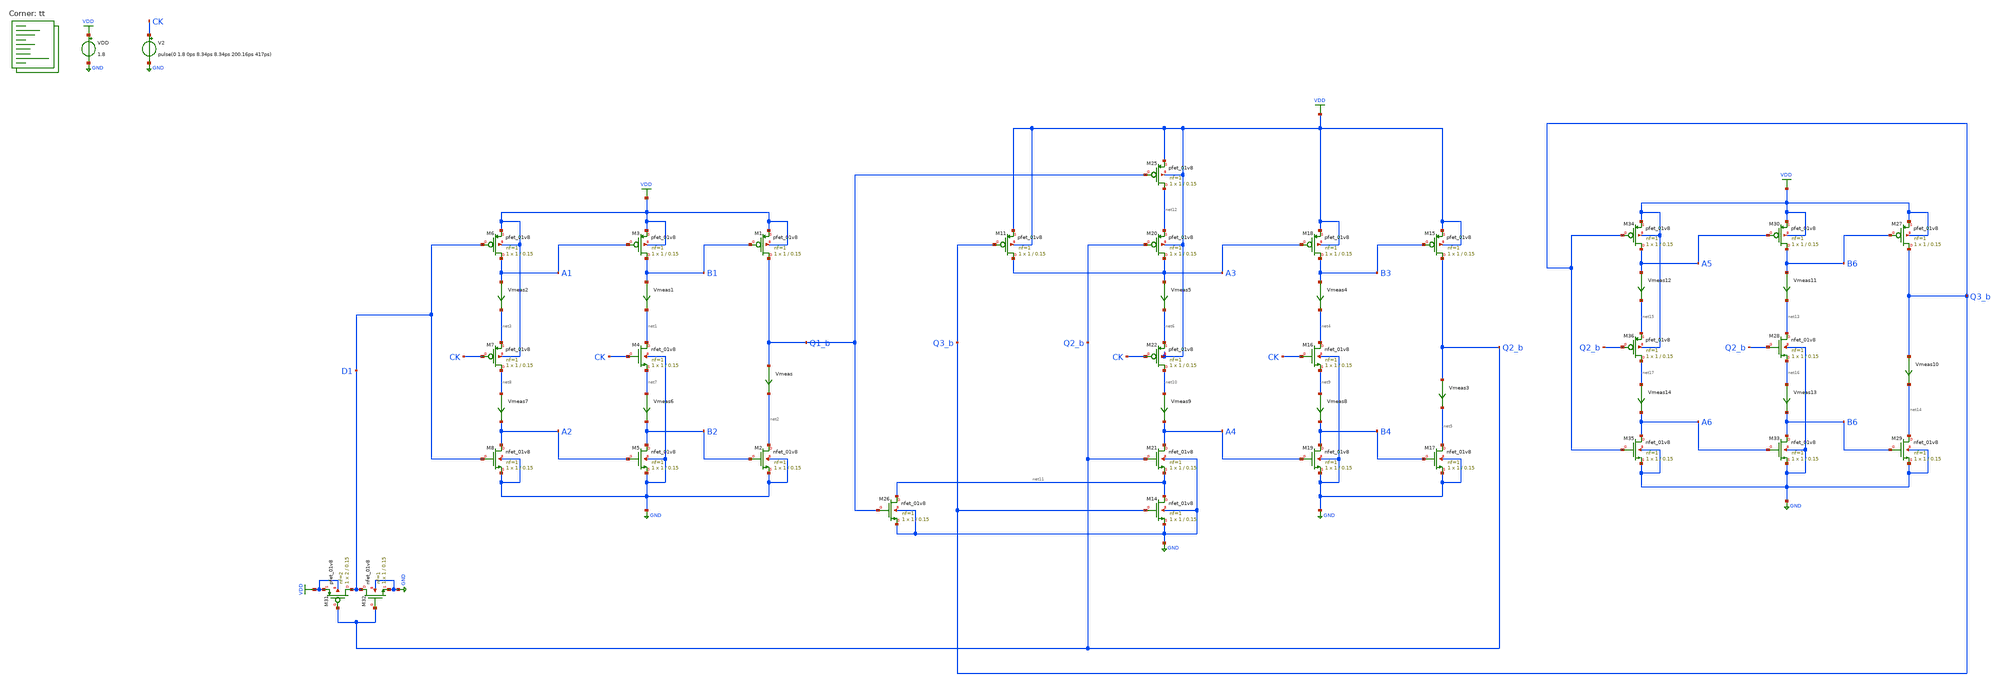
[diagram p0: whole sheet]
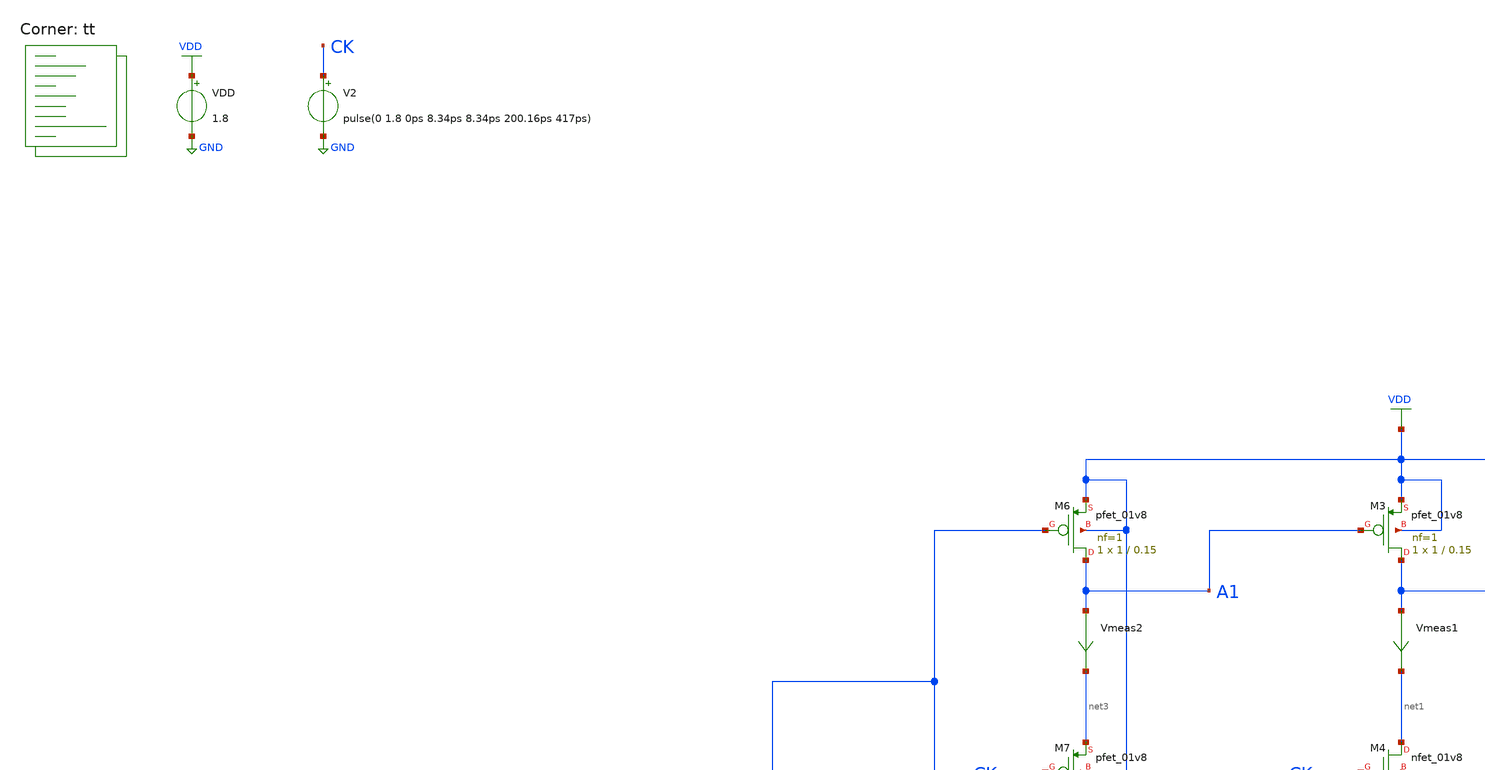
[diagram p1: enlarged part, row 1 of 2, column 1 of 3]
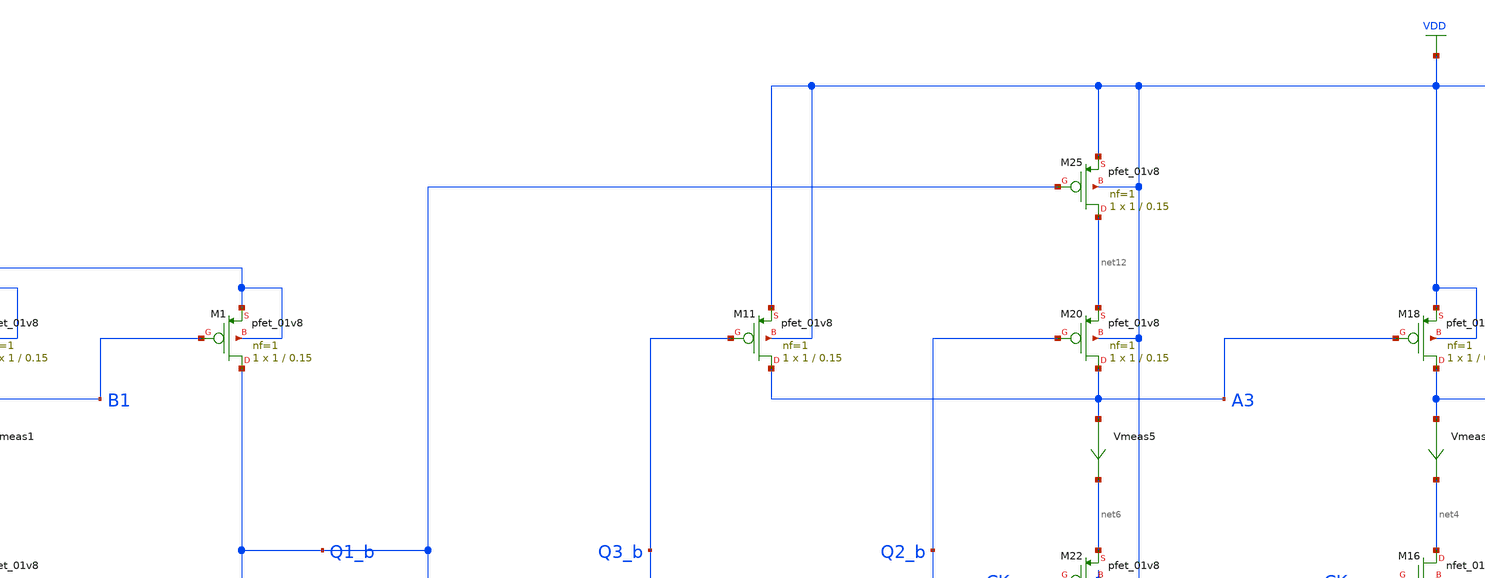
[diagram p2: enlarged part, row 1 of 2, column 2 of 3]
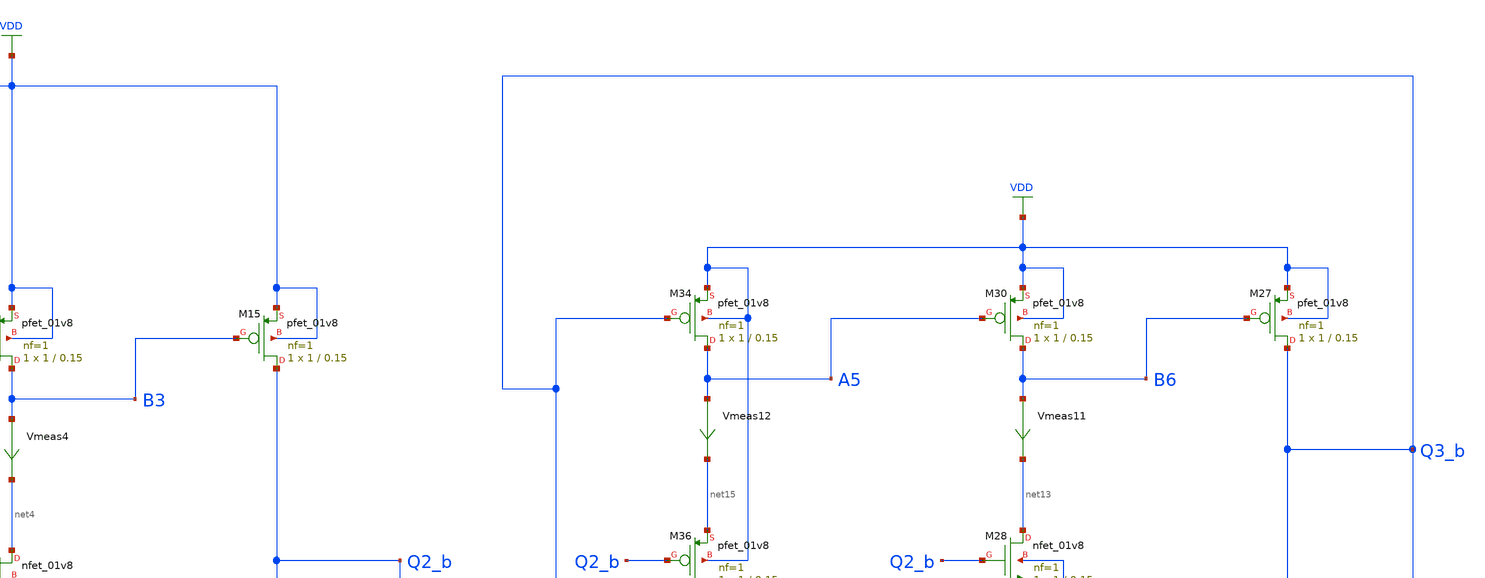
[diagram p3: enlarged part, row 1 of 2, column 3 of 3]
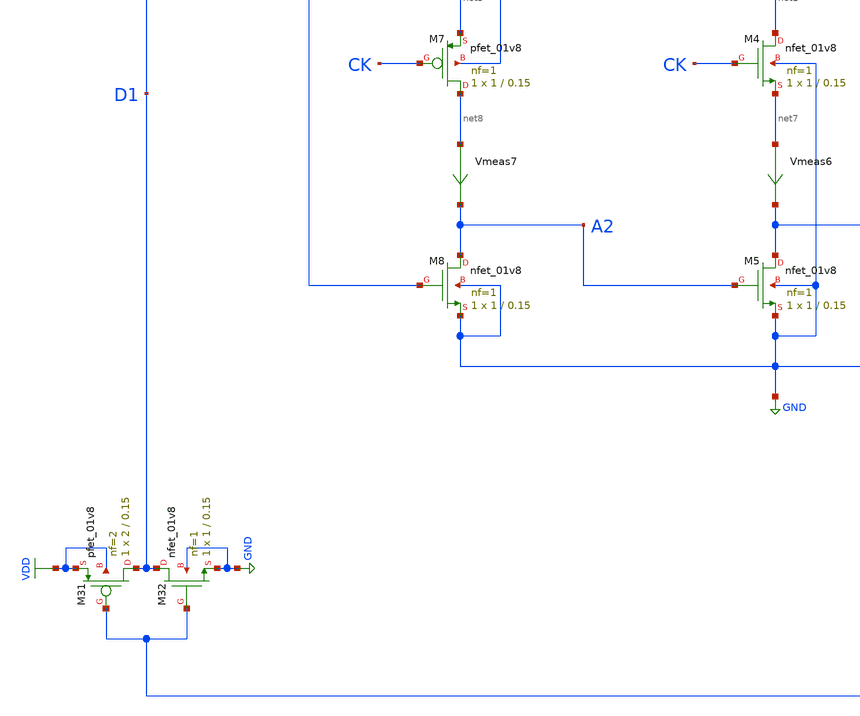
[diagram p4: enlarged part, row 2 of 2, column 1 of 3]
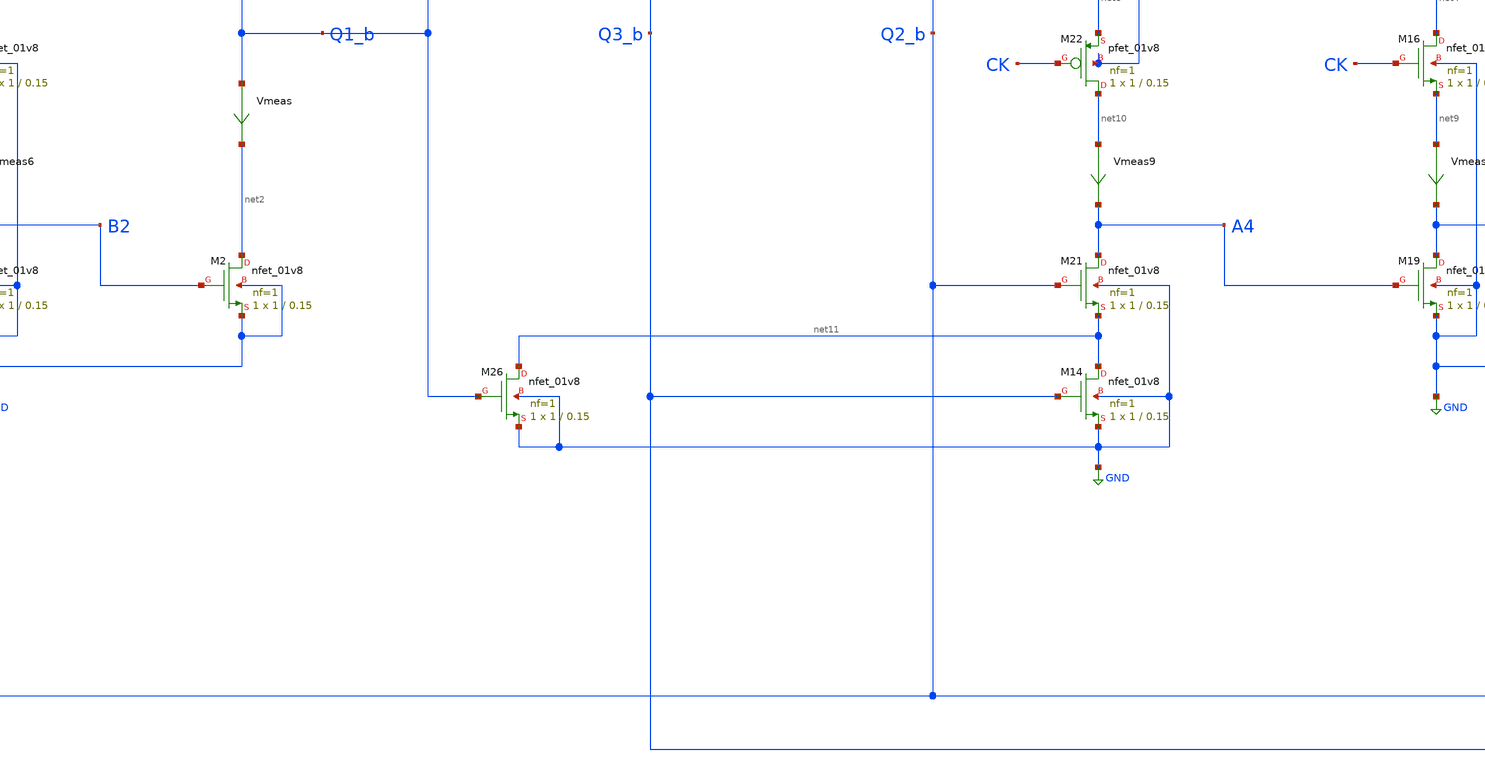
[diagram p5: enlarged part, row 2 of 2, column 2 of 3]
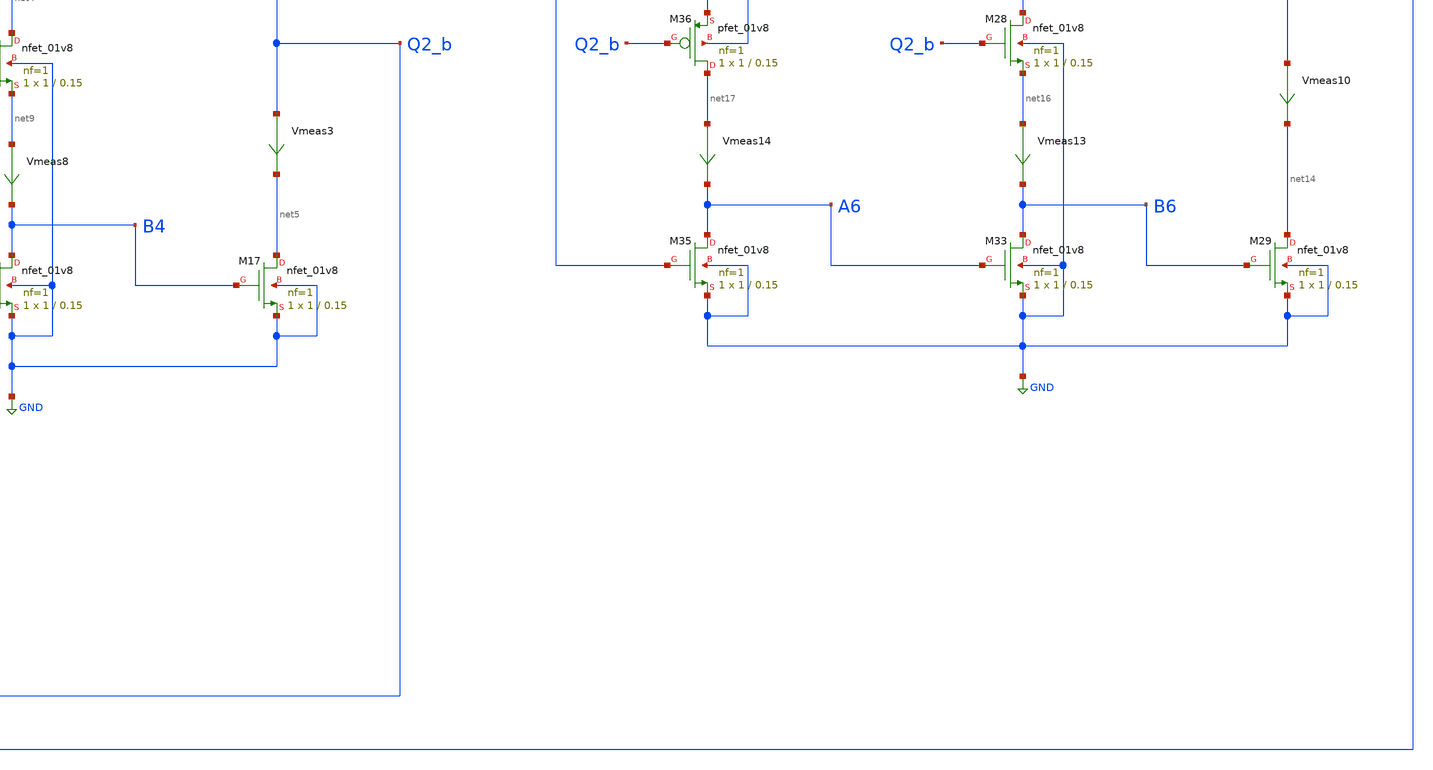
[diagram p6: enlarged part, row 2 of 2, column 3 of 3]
** sch_path: projects/pll/divider/xschem_ngspice/tb_TSPC_FF_comp_sw_divide3_6.sch
**.subckt tb_TSPC_FF_comp_sw_divide3_6
VDD VDD GND 1.8
XM1 Q1_b B1 VDD VDD sky130_fd_pr__pfet_01v8 L=0.15 W=1 nf=1 ad='int((nf+1)/2) * W/nf * 0.29' as='int((nf+2)/2) * W/nf * 0.29'
+ pd='2*int((nf+1)/2) * (W/nf + 0.29)' ps='2*int((nf+2)/2) * (W/nf + 0.29)' nrd='0.29 / W' nrs='0.29 / W'
+ sa=0 sb=0 sd=0 mult=1 m=1
XM4 net1 CK net7 GND sky130_fd_pr__nfet_01v8 L=0.15 W=1 nf=1 ad='int((nf+1)/2) * W/nf * 0.29' as='int((nf+2)/2) * W/nf * 0.29'
+ pd='2*int((nf+1)/2) * (W/nf + 0.29)' ps='2*int((nf+2)/2) * (W/nf + 0.29)' nrd='0.29 / W' nrs='0.29 / W'
+ sa=0 sb=0 sd=0 mult=1 m=1
Vmeas Q1_b net2 0
.save i(vmeas)
XM2 net2 B2 GND GND sky130_fd_pr__nfet_01v8 L=0.15 W=1 nf=1 ad='int((nf+1)/2) * W/nf * 0.29' as='int((nf+2)/2) * W/nf * 0.29'
+ pd='2*int((nf+1)/2) * (W/nf + 0.29)' ps='2*int((nf+2)/2) * (W/nf + 0.29)' nrd='0.29 / W' nrs='0.29 / W'
+ sa=0 sb=0 sd=0 mult=1 m=1
XM3 B1 A1 VDD VDD sky130_fd_pr__pfet_01v8 L=0.15 W=1 nf=1 ad='int((nf+1)/2) * W/nf * 0.29' as='int((nf+2)/2) * W/nf * 0.29'
+ pd='2*int((nf+1)/2) * (W/nf + 0.29)' ps='2*int((nf+2)/2) * (W/nf + 0.29)' nrd='0.29 / W' nrs='0.29 / W'
+ sa=0 sb=0 sd=0 mult=1 m=1
XM5 B2 A2 GND GND sky130_fd_pr__nfet_01v8 L=0.15 W=1 nf=1 ad='int((nf+1)/2) * W/nf * 0.29' as='int((nf+2)/2) * W/nf * 0.29'
+ pd='2*int((nf+1)/2) * (W/nf + 0.29)' ps='2*int((nf+2)/2) * (W/nf + 0.29)' nrd='0.29 / W' nrs='0.29 / W'
+ sa=0 sb=0 sd=0 mult=1 m=1
Vmeas1 B1 net1 0
.save i(vmeas1)
XM6 A1 D1 VDD VDD sky130_fd_pr__pfet_01v8 L=0.15 W=1 nf=1 ad='int((nf+1)/2) * W/nf * 0.29' as='int((nf+2)/2) * W/nf * 0.29'
+ pd='2*int((nf+1)/2) * (W/nf + 0.29)' ps='2*int((nf+2)/2) * (W/nf + 0.29)' nrd='0.29 / W' nrs='0.29 / W'
+ sa=0 sb=0 sd=0 mult=1 m=1
XM8 A2 D1 GND GND sky130_fd_pr__nfet_01v8 L=0.15 W=1 nf=1 ad='int((nf+1)/2) * W/nf * 0.29' as='int((nf+2)/2) * W/nf * 0.29'
+ pd='2*int((nf+1)/2) * (W/nf + 0.29)' ps='2*int((nf+2)/2) * (W/nf + 0.29)' nrd='0.29 / W' nrs='0.29 / W'
+ sa=0 sb=0 sd=0 mult=1 m=1
Vmeas2 A1 net3 0
.save i(vmeas2)
XM7 net8 CK net3 VDD sky130_fd_pr__pfet_01v8 L=0.15 W=1 nf=1 ad='int((nf+1)/2) * W/nf * 0.29' as='int((nf+2)/2) * W/nf * 0.29'
+ pd='2*int((nf+1)/2) * (W/nf + 0.29)' ps='2*int((nf+2)/2) * (W/nf + 0.29)' nrd='0.29 / W' nrs='0.29 / W'
+ sa=0 sb=0 sd=0 mult=1 m=1
XM15 Q2_b B3 VDD VDD sky130_fd_pr__pfet_01v8 L=0.15 W=1 nf=1 ad='int((nf+1)/2) * W/nf * 0.29' as='int((nf+2)/2) * W/nf * 0.29'
+ pd='2*int((nf+1)/2) * (W/nf + 0.29)' ps='2*int((nf+2)/2) * (W/nf + 0.29)' nrd='0.29 / W' nrs='0.29 / W'
+ sa=0 sb=0 sd=0 mult=1 m=1
XM16 net4 CK net9 GND sky130_fd_pr__nfet_01v8 L=0.15 W=1 nf=1 ad='int((nf+1)/2) * W/nf * 0.29' as='int((nf+2)/2) * W/nf * 0.29'
+ pd='2*int((nf+1)/2) * (W/nf + 0.29)' ps='2*int((nf+2)/2) * (W/nf + 0.29)' nrd='0.29 / W' nrs='0.29 / W'
+ sa=0 sb=0 sd=0 mult=1 m=1
Vmeas3 Q2_b net5 0
.save i(vmeas3)
XM17 net5 B4 GND GND sky130_fd_pr__nfet_01v8 L=0.15 W=1 nf=1 ad='int((nf+1)/2) * W/nf * 0.29' as='int((nf+2)/2) * W/nf * 0.29'
+ pd='2*int((nf+1)/2) * (W/nf + 0.29)' ps='2*int((nf+2)/2) * (W/nf + 0.29)' nrd='0.29 / W' nrs='0.29 / W'
+ sa=0 sb=0 sd=0 mult=1 m=1
XM18 B3 A3 VDD VDD sky130_fd_pr__pfet_01v8 L=0.15 W=1 nf=1 ad='int((nf+1)/2) * W/nf * 0.29' as='int((nf+2)/2) * W/nf * 0.29'
+ pd='2*int((nf+1)/2) * (W/nf + 0.29)' ps='2*int((nf+2)/2) * (W/nf + 0.29)' nrd='0.29 / W' nrs='0.29 / W'
+ sa=0 sb=0 sd=0 mult=1 m=1
XM19 B4 A4 GND GND sky130_fd_pr__nfet_01v8 L=0.15 W=1 nf=1 ad='int((nf+1)/2) * W/nf * 0.29' as='int((nf+2)/2) * W/nf * 0.29'
+ pd='2*int((nf+1)/2) * (W/nf + 0.29)' ps='2*int((nf+2)/2) * (W/nf + 0.29)' nrd='0.29 / W' nrs='0.29 / W'
+ sa=0 sb=0 sd=0 mult=1 m=1
Vmeas4 B3 net4 0
.save i(vmeas4)
XM20 A3 Q2_b net12 VDD sky130_fd_pr__pfet_01v8 L=0.15 W=1 nf=1 ad='int((nf+1)/2) * W/nf * 0.29' as='int((nf+2)/2) * W/nf * 0.29'
+ pd='2*int((nf+1)/2) * (W/nf + 0.29)' ps='2*int((nf+2)/2) * (W/nf + 0.29)' nrd='0.29 / W' nrs='0.29 / W'
+ sa=0 sb=0 sd=0 mult=1 m=1
XM21 A4 Q2_b net11 GND sky130_fd_pr__nfet_01v8 L=0.15 W=1 nf=1 ad='int((nf+1)/2) * W/nf * 0.29' as='int((nf+2)/2) * W/nf * 0.29'
+ pd='2*int((nf+1)/2) * (W/nf + 0.29)' ps='2*int((nf+2)/2) * (W/nf + 0.29)' nrd='0.29 / W' nrs='0.29 / W'
+ sa=0 sb=0 sd=0 mult=1 m=1
Vmeas5 A3 net6 0
.save i(vmeas5)
XM22 net10 CK net6 VDD sky130_fd_pr__pfet_01v8 L=0.15 W=1 nf=1 ad='int((nf+1)/2) * W/nf * 0.29' as='int((nf+2)/2) * W/nf * 0.29'
+ pd='2*int((nf+1)/2) * (W/nf + 0.29)' ps='2*int((nf+2)/2) * (W/nf + 0.29)' nrd='0.29 / W' nrs='0.29 / W'
+ sa=0 sb=0 sd=0 mult=1 m=1
Vmeas6 net7 B2 0
.save i(vmeas6)
Vmeas7 net8 A2 0
.save i(vmeas7)
Vmeas8 net9 B4 0
.save i(vmeas8)
Vmeas9 net10 A4 0
.save i(vmeas9)
V2 CK GND pulse(0 1.8 0ps 8.34ps 8.34ps 200.16ps 417ps)
XM31 D1 Q2_b VDD VDD sky130_fd_pr__pfet_01v8 L=0.15 W=2 nf=2 ad='int((nf+1)/2) * W/nf * 0.29' as='int((nf+2)/2) * W/nf * 0.29'
+ pd='2*int((nf+1)/2) * (W/nf + 0.29)' ps='2*int((nf+2)/2) * (W/nf + 0.29)' nrd='0.29 / W' nrs='0.29 / W'
+ sa=0 sb=0 sd=0 mult=1 m=1
XM32 D1 Q2_b GND GND sky130_fd_pr__nfet_01v8 L=0.15 W=1 nf=1 ad='int((nf+1)/2) * W/nf * 0.29' as='int((nf+2)/2) * W/nf * 0.29'
+ pd='2*int((nf+1)/2) * (W/nf + 0.29)' ps='2*int((nf+2)/2) * (W/nf + 0.29)' nrd='0.29 / W' nrs='0.29 / W'
+ sa=0 sb=0 sd=0 mult=1 m=1
XM11 A3 Q3_b VDD VDD sky130_fd_pr__pfet_01v8 L=0.15 W=1 nf=1 ad='int((nf+1)/2) * W/nf * 0.29' as='int((nf+2)/2) * W/nf * 0.29'
+ pd='2*int((nf+1)/2) * (W/nf + 0.29)' ps='2*int((nf+2)/2) * (W/nf + 0.29)' nrd='0.29 / W' nrs='0.29 / W'
+ sa=0 sb=0 sd=0 mult=1 m=1
XM14 net11 Q3_b GND GND sky130_fd_pr__nfet_01v8 L=0.15 W=1 nf=1 ad='int((nf+1)/2) * W/nf * 0.29' as='int((nf+2)/2) * W/nf * 0.29'
+ pd='2*int((nf+1)/2) * (W/nf + 0.29)' ps='2*int((nf+2)/2) * (W/nf + 0.29)' nrd='0.29 / W' nrs='0.29 / W'
+ sa=0 sb=0 sd=0 mult=1 m=1
XM25 net12 Q1_b VDD VDD sky130_fd_pr__pfet_01v8 L=0.15 W=1 nf=1 ad='int((nf+1)/2) * W/nf * 0.29' as='int((nf+2)/2) * W/nf * 0.29'
+ pd='2*int((nf+1)/2) * (W/nf + 0.29)' ps='2*int((nf+2)/2) * (W/nf + 0.29)' nrd='0.29 / W' nrs='0.29 / W'
+ sa=0 sb=0 sd=0 mult=1 m=1
XM26 net11 Q1_b GND GND sky130_fd_pr__nfet_01v8 L=0.15 W=1 nf=1 ad='int((nf+1)/2) * W/nf * 0.29' as='int((nf+2)/2) * W/nf * 0.29'
+ pd='2*int((nf+1)/2) * (W/nf + 0.29)' ps='2*int((nf+2)/2) * (W/nf + 0.29)' nrd='0.29 / W' nrs='0.29 / W'
+ sa=0 sb=0 sd=0 mult=1 m=1
XM27 Q3_b B6 VDD VDD sky130_fd_pr__pfet_01v8 L=0.15 W=1 nf=1 ad='int((nf+1)/2) * W/nf * 0.29' as='int((nf+2)/2) * W/nf * 0.29'
+ pd='2*int((nf+1)/2) * (W/nf + 0.29)' ps='2*int((nf+2)/2) * (W/nf + 0.29)' nrd='0.29 / W' nrs='0.29 / W'
+ sa=0 sb=0 sd=0 mult=1 m=1
XM28 net13 Q2_b net16 GND sky130_fd_pr__nfet_01v8 L=0.15 W=1 nf=1 ad='int((nf+1)/2) * W/nf * 0.29' as='int((nf+2)/2) * W/nf * 0.29'
+ pd='2*int((nf+1)/2) * (W/nf + 0.29)' ps='2*int((nf+2)/2) * (W/nf + 0.29)' nrd='0.29 / W' nrs='0.29 / W'
+ sa=0 sb=0 sd=0 mult=1 m=1
Vmeas10 Q3_b net14 0
.save i(vmeas10)
XM29 net14 B6 GND GND sky130_fd_pr__nfet_01v8 L=0.15 W=1 nf=1 ad='int((nf+1)/2) * W/nf * 0.29' as='int((nf+2)/2) * W/nf * 0.29'
+ pd='2*int((nf+1)/2) * (W/nf + 0.29)' ps='2*int((nf+2)/2) * (W/nf + 0.29)' nrd='0.29 / W' nrs='0.29 / W'
+ sa=0 sb=0 sd=0 mult=1 m=1
XM30 B6 A5 VDD VDD sky130_fd_pr__pfet_01v8 L=0.15 W=1 nf=1 ad='int((nf+1)/2) * W/nf * 0.29' as='int((nf+2)/2) * W/nf * 0.29'
+ pd='2*int((nf+1)/2) * (W/nf + 0.29)' ps='2*int((nf+2)/2) * (W/nf + 0.29)' nrd='0.29 / W' nrs='0.29 / W'
+ sa=0 sb=0 sd=0 mult=1 m=1
XM33 B6 A6 GND GND sky130_fd_pr__nfet_01v8 L=0.15 W=1 nf=1 ad='int((nf+1)/2) * W/nf * 0.29' as='int((nf+2)/2) * W/nf * 0.29'
+ pd='2*int((nf+1)/2) * (W/nf + 0.29)' ps='2*int((nf+2)/2) * (W/nf + 0.29)' nrd='0.29 / W' nrs='0.29 / W'
+ sa=0 sb=0 sd=0 mult=1 m=1
Vmeas11 B6 net13 0
.save i(vmeas11)
XM34 A5 Q3_b VDD VDD sky130_fd_pr__pfet_01v8 L=0.15 W=1 nf=1 ad='int((nf+1)/2) * W/nf * 0.29' as='int((nf+2)/2) * W/nf * 0.29'
+ pd='2*int((nf+1)/2) * (W/nf + 0.29)' ps='2*int((nf+2)/2) * (W/nf + 0.29)' nrd='0.29 / W' nrs='0.29 / W'
+ sa=0 sb=0 sd=0 mult=1 m=1
XM35 A6 Q3_b GND GND sky130_fd_pr__nfet_01v8 L=0.15 W=1 nf=1 ad='int((nf+1)/2) * W/nf * 0.29' as='int((nf+2)/2) * W/nf * 0.29'
+ pd='2*int((nf+1)/2) * (W/nf + 0.29)' ps='2*int((nf+2)/2) * (W/nf + 0.29)' nrd='0.29 / W' nrs='0.29 / W'
+ sa=0 sb=0 sd=0 mult=1 m=1
Vmeas12 A5 net15 0
.save i(vmeas12)
XM36 net17 Q2_b net15 VDD sky130_fd_pr__pfet_01v8 L=0.15 W=1 nf=1 ad='int((nf+1)/2) * W/nf * 0.29' as='int((nf+2)/2) * W/nf * 0.29'
+ pd='2*int((nf+1)/2) * (W/nf + 0.29)' ps='2*int((nf+2)/2) * (W/nf + 0.29)' nrd='0.29 / W' nrs='0.29 / W'
+ sa=0 sb=0 sd=0 mult=1 m=1
Vmeas13 net16 B6 0
.save i(vmeas13)
Vmeas14 net17 A6 0
.save i(vmeas14)
**** begin user architecture code



.include /foss/pdks/sky130A/libs.ref/sky130_fd_sc_hd/spice/sky130_fd_sc_hd.spice

.option method=gear
.option wnflag=1
.option savecurrents

.save @m.xm1.msky130_fd_pr__pfet_01v8[gm] @m.xm2.msky130_fd_pr__nfet_01v8[gm] @m.xm3.msky130_fd_pr__pfet_01v8[gm] @m.xm4.msky130_fd_pr__nfet_01v8[gm] @m.xm4_c.msky130_fd_pr__pfet_01v8[gm] @m.xm5.msky130_fd_pr__nfet_01v8[gm] @m.xm6.msky130_fd_pr__pfet_01v8[gm] @m.xm7.msky130_fd_pr__pfet_01v8[gm] @m.xm7_c.msky130_fd_pr__nfet_01v8[gm] @m.xm8.msky130_fd_pr__nfet_01v8[gm]

*.ic v(d)=0
*.ic v(q)=0
*.ic v(q1)=0

.control

  save v(d1) v(q1_b) v(q2_b) v(q3_b) v(a1) v(a2) v(a3) v(a4) v(a5) v(a6) v(b1) v(b2) v(b3) v(b4)
+ v(b5) v(b6) v(ck) v(ck1) v(ck1_b) v(ck2) v(ck2_b)
  * save all
  * tran 0.1n 1u
  tran 1p 30n

  remzerovec
  write tb_TSPC_FF_comp_sw_divide3_5.raw
  * set appendwrite

.endc



.lib $::SKYWATER_MODELS/sky130.lib.spice tt
**** end user architecture code
**.ends
.GLOBAL GND
.GLOBAL VDD
.end
